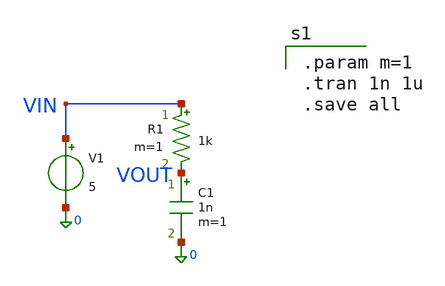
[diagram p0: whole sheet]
** sch_path: tests/golden/SCHEM/cases/SCHEM-NL-01/input/SC_Test.sch
**.subckt SC_Test
V1 VIN 0 5
R1 VIN VOUT 1k m=1
C1 VOUT 0 1n m=1
**** begin user architecture code

.param m=1
.tran 1n 1u
.save all

**** end user architecture code
**.ends
.end
